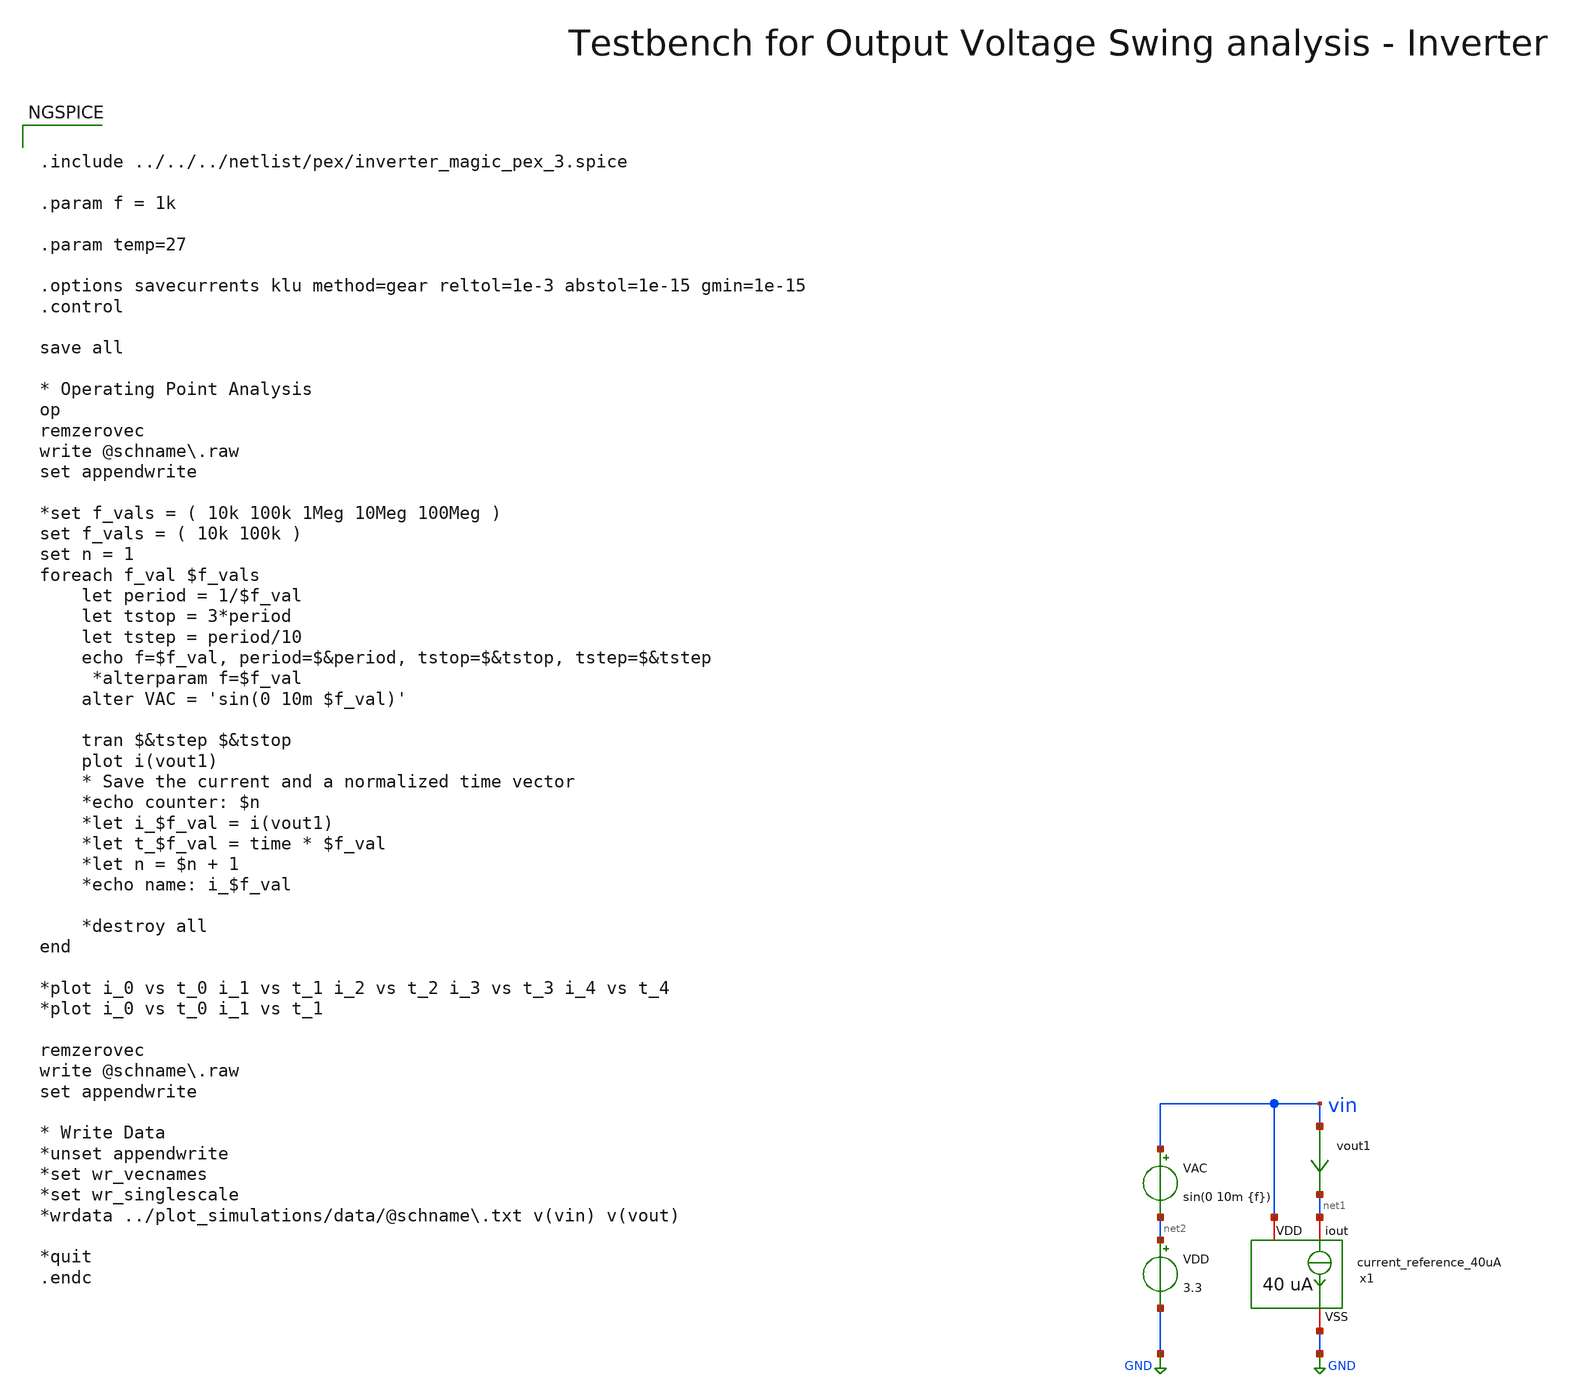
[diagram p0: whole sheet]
** sch_path: macros/heichips26_vcr/macros/switched_capacitor/testbenches/xschem/tb_current_reference_tran.sch
**.subckt tb_current_reference_tran
VDD net2 GND 3.3
vout1 vin net1 0
.save i(vout1)
x1 vin net1 GND current_reference_40uA
VAC vin net2 sin(0 10m {f})
**** begin user architecture code


.include ../../../netlist/pex/inverter_magic_pex_3.spice

.param f = 1k

.param temp=27

.options savecurrents klu method=gear reltol=1e-3 abstol=1e-15 gmin=1e-15
.control

save all

* Operating Point Analysis
op
remzerovec
write @schname\.raw
set appendwrite

*set f_vals = ( 10k 100k 1Meg 10Meg 100Meg )
set f_vals = ( 10k 100k )
set n = 1
foreach f_val $f_vals
	let period = 1/$f_val
	let tstop = 3*period
	let tstep = period/10
	echo f=$f_val, period=$&period, tstop=$&tstop, tstep=$&tstep
 	*alterparam f=$f_val
	alter VAC = 'sin(0 10m $f_val)'

	tran $&tstep $&tstop
	plot i(vout1)
	* Save the current and a normalized time vector
	*echo counter: $n
	*let i_$f_val = i(vout1)
	*let t_$f_val = time * $f_val
	*let n = $n + 1
	*echo name: i_$f_val

	*destroy all
end

*plot i_0 vs t_0 i_1 vs t_1 i_2 vs t_2 i_3 vs t_3 i_4 vs t_4
*plot i_0 vs t_0 i_1 vs t_1

remzerovec
write @schname\.raw
set appendwrite

* Write Data
*unset appendwrite
*set wr_vecnames
*set wr_singlescale
*wrdata ../plot_simulations/data/@schname\.txt v(vin) v(vout)

*quit
.endc



.lib cornerMOSlv.lib mos_tt
.lib cornerMOShv.lib mos_tt
.lib cornerRES.lib res_typ
.lib cornerDIO.lib dio_tt

**** end user architecture code
**.ends

* expanding   symbol:  current_reference_40uA.sym # of pins=3
** sym_path: macros/heichips26_vcr/macros/switched_capacitor/schematic/xschem/current_reference_40uA.sym
** sch_path: macros/heichips26_vcr/macros/switched_capacitor/schematic/xschem/current_reference_40uA.sch
.subckt current_reference_40uA VDD iout VSS
*.iopin VSS
*.iopin VDD
*.iopin iout
XM8 net2 net2 VSS VSS sg13_hv_nmos w=n_w l=n_l ng=1 m=1 mm_ok=1
XM6 net2 net1 VDD VDD sg13_hv_pmos w=p_w l=p_l ng=1 m=1 mm_ok=1
XM1 net1 net1 VDD VDD sg13_hv_pmos w=p_w l=p_l ng=1 m=1 mm_ok=1
XM3 net1 net2 net3 VSS sg13_hv_nmos w=n_w l=n_l ng=1 m=1 mm_ok=1
XR2 net4 VSS VSS rppd w=2e-6 l=21.9e-6 m=1 b=0 mm_ok=1
XM2 net1 net2 net3 VSS sg13_hv_nmos w=n_w l=n_l ng=1 m=1 mm_ok=1
XM4 net1 net2 net3 VSS sg13_hv_nmos w=n_w l=n_l ng=1 m=1 mm_ok=1
XM5 net1 net2 net3 VSS sg13_hv_nmos w=n_w l=n_l ng=1 m=1 mm_ok=1
XM7 iout net2 VSS VSS sg13_hv_nmos w=n_w l=n_l ng=1 m=1 mm_ok=1
XR3 net3 net4 VSS rsil w=0.5e-6 l=365e-6 m=1 mm_ok=1
**** begin user architecture code


.param n_w = 6u
.param n_l = 5u
.param p_w = 10u
.param p_l = 2u


**** end user architecture code
.ends

.GLOBAL GND
.end
